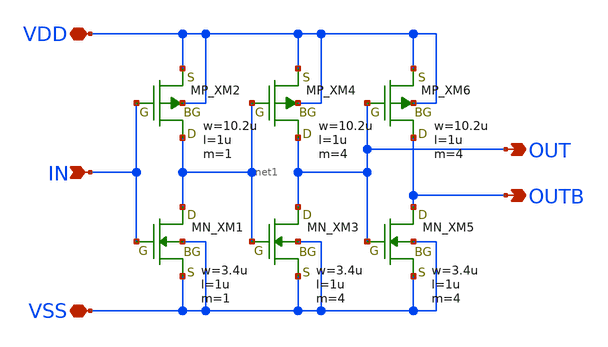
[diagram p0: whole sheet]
** sch_path: member_project/imager/YuMaehashi/design/hsc_buf.sch
**.subckt hsc_buf VSS IN OUT VDD OUTB
*.iopin VSS
*.ipin IN
*.opin OUT
*.iopin VDD
*.opin OUTB
XXM1 net1 IN VSS VSS NMOS w=3.4u l=1u nrd=0 nrs=0 m=1
XXM2 net1 IN VDD VDD PMOS w=10.2u l=1u nrd=0 nrs=0 m=1
XXM3 OUT net1 VSS VSS NMOS w=3.4u l=1u nrd=0 nrs=0 m=4
XXM4 OUT net1 VDD VDD PMOS w=10.2u l=1u nrd=0 nrs=0 m=4
XXM5 OUTB OUT VSS VSS NMOS w=3.4u l=1u nrd=0 nrs=0 m=4
XXM6 OUTB OUT VDD VDD PMOS w=10.2u l=1u nrd=0 nrs=0 m=4
**.ends
.end
